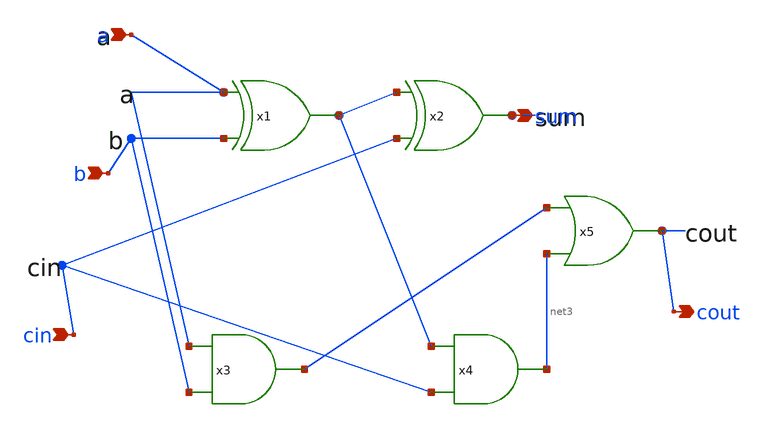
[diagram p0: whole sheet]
** sch_path: full_adder_1bit.sch
* StefanSchippers/xschem/xschem_library/ngspice/and_ngspice.sch:
* Copyright (C) 1998-2023 Stefan Frederik Schippers
* This program is free software; you can redistribute it and/or modify
* it under the terms of the GNU General Public License as published by
* the Free Software Foundation; either version 2 of the License, or
* (at your option) any later version.
**.subckt full_adder_1bit a b cin sum cout
*.ipin a
*.ipin b
*.ipin cin
*.opin sum
*.opin cout
x1 net1 a b xor_ngspice ROUT=1000
x2 sum net1 cin xor_ngspice ROUT=1000
x5 cout net2 net3 or_ngspice ROUT=1000
x3 net2 a b and_ngspice ROUT=1000
x4 net3 net1 cin and_ngspice ROUT=1000
**.ends

* expanding   symbol:  xor_ngspice.sym # of pins=3
** sym_path: xor_ngspice.sym
** sch_path: xor_ngspice.sch
.subckt xor_ngspice Y A B  ROUT=1000
*.ipin A
*.opin Y
*.ipin B
B1 net1 0 V = 'VCC/2*(1+tanh((abs(V(A1)-V(B1))-VCC/2)*100))'
R1 Y1 net1 'ROUT' m=1
C1 A1 0 8f m=1
C2 B1 0 8f m=1
C3 Y1 0 8f m=1
V1 A1 A 0
V2 B1 B 0
V3 Y Y1 0
.ends


* expanding   symbol:  or_ngspice.sym # of pins=3
** sym_path: or_ngspice.sym
** sch_path: or_ngspice.sch
.subckt or_ngspice Y A B  ROUT=1000
*.ipin A
*.opin Y
*.ipin B
B1 net1 0 V = 'VCC/2*(1+tanh((max(V(A1),V(B1))-VCC/2)*100))'
R1 Y1 net1 'ROUT' m=1
C1 A1 0 8f m=1
C2 B1 0 8f m=1
C3 Y1 0 8f m=1
V1 A1 A 0
V2 B1 B 0
V3 Y Y1 0
.ends


* expanding   symbol:  and_ngspice.sym # of pins=3
** sym_path: and_ngspice.sym
** sch_path: and_ngspice.sch
.subckt and_ngspice Y A B  ROUT=1000
*.ipin A
*.opin Y
*.ipin B
B1 net1 0 V = 'VCC/2*(1+tanh((min(V(A1),V(B1))-VCC/2)*100))'
R1 Y1 net1 'ROUT' m=1
C1 A1 0 8f m=1
C2 B1 0 8f m=1
C3 Y1 0 8f m=1
V1 A1 A 0
V2 B1 B 0
V3 Y Y1 0
.ends

.end
